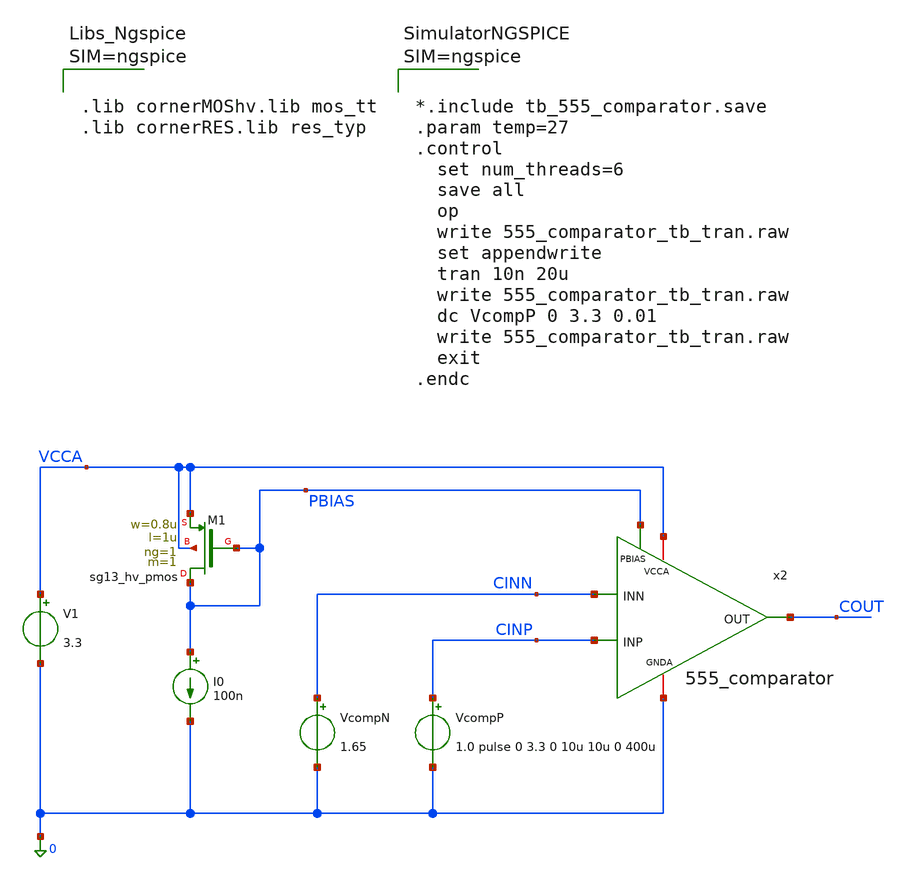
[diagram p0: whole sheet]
** sch_path: macros/heichips26_FAIf/macros/comparator/testbenches/xschem/555_comparator_tb_tran.sch
**.subckt 555_comparator_tb_tran
x2 VCCA PBIAS COUT CINN CINP 0 555_comparator
V1 VCCA 0 3.3
VcompN CINN 0 1.65
VcompP CINP 0 1.0 pulse 0 3.3 0 10u 10u 0 400u
I0 PBIAS 0 100n
XM1 PBIAS PBIAS VCCA VCCA sg13_hv_pmos w=0.8u l=1u ng=1 m=1 mm_ok=1
**** begin user architecture code



.lib cornerMOShv.lib mos_tt
.lib cornerRES.lib res_typ






*.include tb_555_comparator.save
.param temp=27
.control
  set num_threads=6
  save all
  op
  write 555_comparator_tb_tran.raw
  set appendwrite
  tran 10n 20u
  write 555_comparator_tb_tran.raw
  dc VcompP 0 3.3 0.01
  write 555_comparator_tb_tran.raw
  exit
.endc



**** end user architecture code
**.ends

* expanding   symbol:  555_comparator.sym # of pins=6
** sym_path: macros/heichips26_FAIf/macros/comparator/schematic/xschem/555_comparator.sym
** sch_path: macros/heichips26_FAIf/macros/comparator/schematic/xschem/555_comparator.sch
.subckt 555_comparator VCCA PBIAS OUT INN INP GNDA
*.ipin INP
*.iopin VCCA
*.opin OUT
*.iopin GNDA
*.ipin INN
*.ipin PBIAS
XMP1 usource PBIAS VCCA VCCA sg13_hv_pmos w=0.8u l=1u ng=1 m=1 mm_ok=1
XMN1 diff diff GNDA GNDA sg13_hv_nmos w=0.4u l=1u ng=1 m=1 mm_ok=1
XMN2 gmn1 diff GNDA GNDA sg13_hv_nmos w=0.4u l=1u ng=1 m=1 mm_ok=1
XMP4 gmn1 INP usource VCCA sg13_hv_pmos w=5u l=0.45u ng=1 m=2 mm_ok=1
XMP3 diff INN usource VCCA sg13_hv_pmos w=5u l=0.45u ng=1 m=2 mm_ok=1
XMP2 cout_stage PBIAS VCCA VCCA sg13_hv_pmos w=0.8u l=1u ng=1 m=1 mm_ok=1
XMN3 cout_stage gmn1 GNDA GNDA sg13_hv_nmos w=2.4u l=0.45u ng=1 m=1 mm_ok=1
XMN4 inv_stage cout_stage GNDA GNDA sg13_hv_nmos w=0.3u l=0.45u ng=1 m=1 mm_ok=1
XMP5 inv_stage cout_stage VCCA VCCA sg13_hv_pmos w=0.6u l=0.45u ng=1 m=1 mm_ok=1
XMN5 OUT inv_stage GNDA GNDA sg13_hv_nmos w=0.3u l=0.45u ng=1 m=2 mm_ok=1
XMP6 OUT inv_stage VCCA VCCA sg13_hv_pmos w=0.6u l=0.45u ng=1 m=2 mm_ok=1
XMPdum1 VCCA VCCA VCCA VCCA sg13_hv_pmos w=0.8u l=1u ng=1 m=2 mm_ok=1
XMPdum2 VCCA VCCA VCCA VCCA sg13_hv_pmos w=2.5u l=0.45u ng=1 m=8 mm_ok=1
XMPdum3 VCCA VCCA VCCA VCCA sg13_hv_pmos w=5u l=0.45u ng=1 m=4 mm_ok=1
XMNdum2 GNDA GNDA GNDA GNDA sg13_hv_nmos w=1.2u l=0.45u ng=1 m=2 mm_ok=1
XMNdum1 GNDA GNDA GNDA GNDA sg13_hv_nmos w=0.4u l=1u ng=1 m=2 mm_ok=1
.ends

.end
